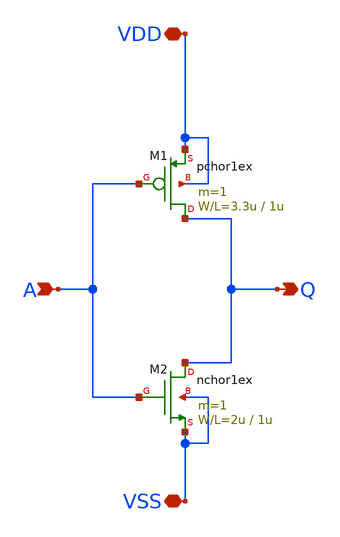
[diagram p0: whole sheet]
** sch_path: member_project/KentoKashiuchi0821Kento/0811_ishi_Netlist.sch
**.subckt 0811_ishi_Netlist A Q VDD VSS
*.ipin A
*.opin Q
*.iopin VDD
*.iopin VSS
M1 Q A VDD VDD pchor1ex L=1u W=3.3u m=1
M2 Q A VSS VSS nchor1ex L=1u W=2u m=1
**.ends
.end
